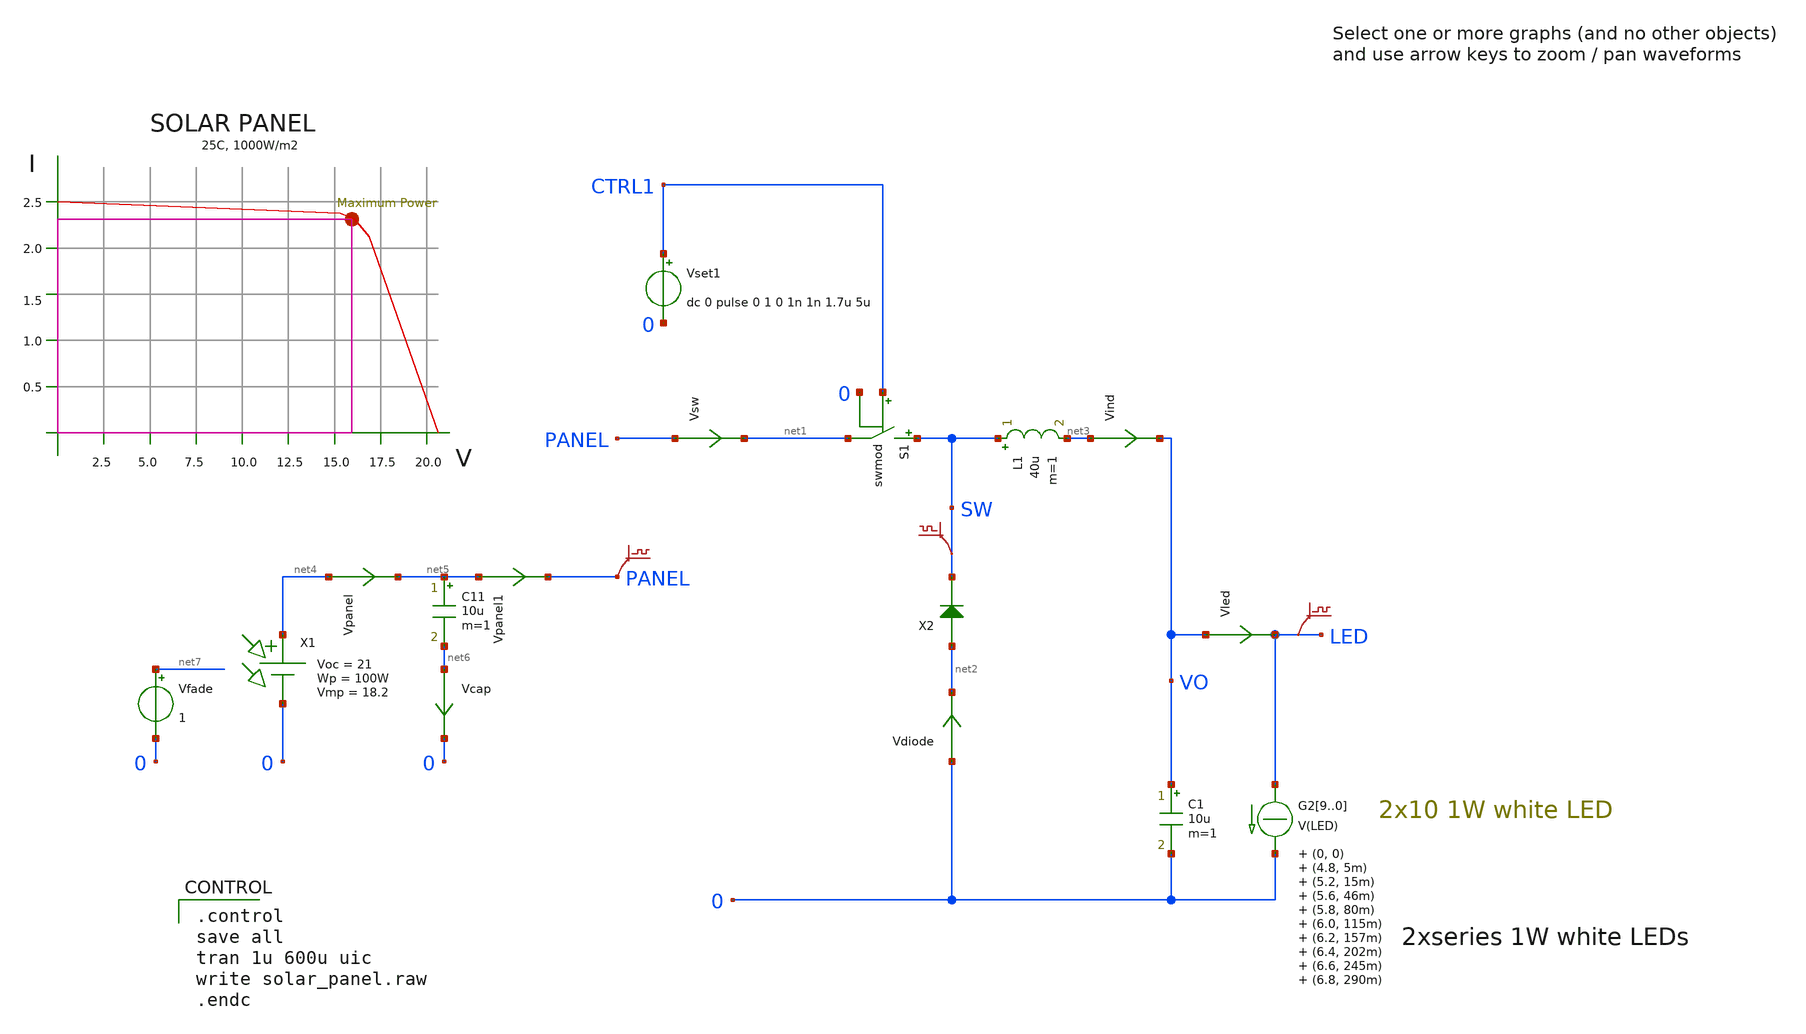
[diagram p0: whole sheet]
** sch_path: xschem_library/ngspice/solar_panel.sch
* xschem_library/ngspice/diode_ngspice.sch:
* Copyright (C) 1998-2023 Stefan Frederik Schippers
* This program is free software; you can redistribute it and/or modify
* it under the terms of the GNU General Public License as published by
* the Free Software Foundation; either version 2 of the License, or
* (at your option) any later version.
**.subckt solar_panel
Vled VO LED 0
.save i(vled)
L1 SW net3 40u m=1
C1 VO 0 10u m=1
Vset1 CTRL1 0 dc 0 pulse 0 1 0 1n 1n 1.7u 5u
Vind net3 VO 0
.save i(vind)
G29 LED 0 TABLE { V(LED) } = (0, 0) (4.8, 5m) (5.2, 15m) (5.6, 46m) (5.8, 80m) (6.0, 115m) (6.2, 157m)
+ (6.4, 202m) (6.6, 245m) (6.8, 290m) (7.0, 337m) (7.2, 395m) (7.4, 470m) (8.0, 750m)
G28 LED 0 TABLE { V(LED) } = (0, 0) (4.8, 5m) (5.2, 15m) (5.6, 46m) (5.8, 80m) (6.0, 115m) (6.2, 157m)
+ (6.4, 202m) (6.6, 245m) (6.8, 290m) (7.0, 337m) (7.2, 395m) (7.4, 470m) (8.0, 750m)
G27 LED 0 TABLE { V(LED) } = (0, 0) (4.8, 5m) (5.2, 15m) (5.6, 46m) (5.8, 80m) (6.0, 115m) (6.2, 157m)
+ (6.4, 202m) (6.6, 245m) (6.8, 290m) (7.0, 337m) (7.2, 395m) (7.4, 470m) (8.0, 750m)
G26 LED 0 TABLE { V(LED) } = (0, 0) (4.8, 5m) (5.2, 15m) (5.6, 46m) (5.8, 80m) (6.0, 115m) (6.2, 157m)
+ (6.4, 202m) (6.6, 245m) (6.8, 290m) (7.0, 337m) (7.2, 395m) (7.4, 470m) (8.0, 750m)
G25 LED 0 TABLE { V(LED) } = (0, 0) (4.8, 5m) (5.2, 15m) (5.6, 46m) (5.8, 80m) (6.0, 115m) (6.2, 157m)
+ (6.4, 202m) (6.6, 245m) (6.8, 290m) (7.0, 337m) (7.2, 395m) (7.4, 470m) (8.0, 750m)
G24 LED 0 TABLE { V(LED) } = (0, 0) (4.8, 5m) (5.2, 15m) (5.6, 46m) (5.8, 80m) (6.0, 115m) (6.2, 157m)
+ (6.4, 202m) (6.6, 245m) (6.8, 290m) (7.0, 337m) (7.2, 395m) (7.4, 470m) (8.0, 750m)
G23 LED 0 TABLE { V(LED) } = (0, 0) (4.8, 5m) (5.2, 15m) (5.6, 46m) (5.8, 80m) (6.0, 115m) (6.2, 157m)
+ (6.4, 202m) (6.6, 245m) (6.8, 290m) (7.0, 337m) (7.2, 395m) (7.4, 470m) (8.0, 750m)
G22 LED 0 TABLE { V(LED) } = (0, 0) (4.8, 5m) (5.2, 15m) (5.6, 46m) (5.8, 80m) (6.0, 115m) (6.2, 157m)
+ (6.4, 202m) (6.6, 245m) (6.8, 290m) (7.0, 337m) (7.2, 395m) (7.4, 470m) (8.0, 750m)
G21 LED 0 TABLE { V(LED) } = (0, 0) (4.8, 5m) (5.2, 15m) (5.6, 46m) (5.8, 80m) (6.0, 115m) (6.2, 157m)
+ (6.4, 202m) (6.6, 245m) (6.8, 290m) (7.0, 337m) (7.2, 395m) (7.4, 470m) (8.0, 750m)
G20 LED 0 TABLE { V(LED) } = (0, 0) (4.8, 5m) (5.2, 15m) (5.6, 46m) (5.8, 80m) (6.0, 115m) (6.2, 157m)
+ (6.4, 202m) (6.6, 245m) (6.8, 290m) (7.0, 337m) (7.2, 395m) (7.4, 470m) (8.0, 750m)
Vsw PANEL net1 0
.save i(vsw)
Vdiode 0 net2 0
.save i(vdiode)
.save v(led)
.save v(panel)
.save v(sw)
X1 net4 0 pv_ngspice R1=0.1 R2=10 Vmp=17 Voc=21 m=1
C11 net5 net6 10u m=1
Vpanel net4 net5 0
.save i(vpanel)
X2 net2 SW diode_ngspice Ron=0.1 Roff=1e9 m=1
S1 SW net1 CTRL1 0 swmod
Vpanel1 net5 PANEL 0
.save i(vpanel1)
Vcap net6 0 0
.save i(vcap)
Vfade net7 0 1
**** begin user architecture code

.control
save all
tran 1u 600u uic
write solar_panel.raw
.endc




.MODEL DIODE D(IS=1.139e-08 RS=0.99 CJO=9.3e-12 VJ=1.6 M=0.411 BV=30 EG=0.7 )
.MODEL swmod SW(VT=0.5 VH=0.01 RON=0.01 ROFF=10000000)


**** end user architecture code
**.ends

* expanding   symbol:  pv_ngspice.sym # of pins=2
** sym_path: xschem_library/ngspice/pv_ngspice.sym
** sch_path: xschem_library/ngspice/pv_ngspice.sch
.subckt pv_ngspice plus minus   R1=0.1 R2=10 Vmp=17 Voc=21
*.iopin plus
*.iopin minus
Vm minus mn 0
.save i(vm)
B1 mn pn I = pwl(V(pn,mn), 0, 6.3, 18, 5.7, 18.3, 5.6, 18.6, 5.4, 18.9, 5.1, 19.5, 4.0, 21, 0, 22,
+ 0)
R1 pn mn 500000 m=1
R2 plus pn 0.1 m=1
.ends


* expanding   symbol:  diode_ngspice.sym # of pins=2
** sym_path: xschem_library/ngspice/diode_ngspice.sym
** sch_path: xschem_library/ngspice/diode_ngspice.sch
.subckt diode_ngspice plus minus   Roff=1e9 Ron=0.1
*.iopin plus
*.iopin minus
Vm mn minus 0
.save i(vm)
Vp plus pn 0
.save i(vp)
B1 pn mn I = 'v(pn,mn) > 0 ? v(pn,mn) / Ron : v(pn,mn) / Roff'
.ends

.end
